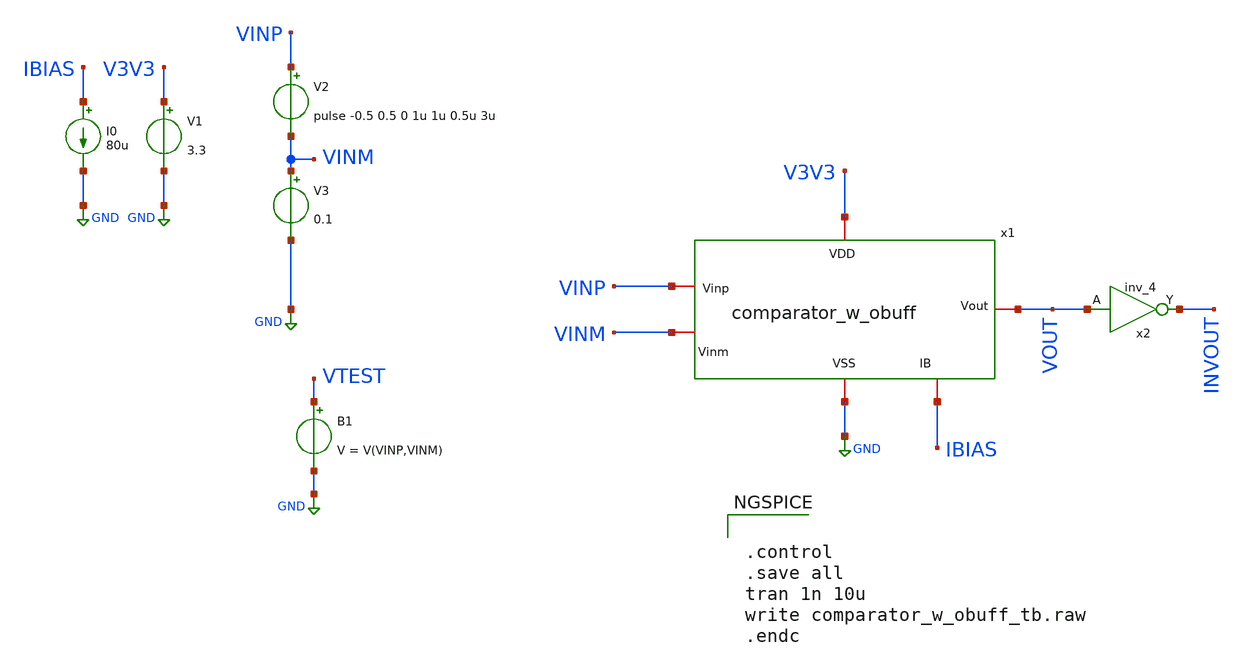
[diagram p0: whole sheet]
** sch_path: design/comparator/comparator_w_obuff_tb.sch
**.subckt comparator_w_obuff_tb
V1 V3V3 GND 3.3
I0 IBIAS GND 80u
V3 VINM GND 0.1
V2 VINP VINM pulse -0.5 0.5 0 1u 1u 0.5u 3u
x2 VOUT GND GND V3V3 V3V3 INVOUT sky130_fd_sc_hvl__inv_4
B1 VTEST GND V = V(VINP,VINM)
x1 V3V3 GND VOUT VINP VINM IBIAS comparator_w_obuff
**** begin user architecture code

.include $::SKYWATER_MODELS/cells/nfet_01v8/sky130_fd_pr__nfet_01v8__tt.corner.spice
.include $::SKYWATER_MODELS/cells/nfet_01v8_lvt/sky130_fd_pr__nfet_01v8_lvt__tt.corner.spice
.include $::SKYWATER_MODELS/cells/pfet_01v8/sky130_fd_pr__pfet_01v8__tt.corner.spice
.include $::SKYWATER_MODELS/cells/nfet_03v3_nvt/sky130_fd_pr__nfet_03v3_nvt__tt.corner.spice
.include $::SKYWATER_MODELS/cells/nfet_05v0_nvt/sky130_fd_pr__nfet_05v0_nvt__tt.corner.spice
.include $::SKYWATER_MODELS/cells/esd_nfet_01v8/sky130_fd_pr__esd_nfet_01v8__tt.corner.spice
.include $::SKYWATER_MODELS/cells/pfet_01v8_lvt/sky130_fd_pr__pfet_01v8_lvt__tt.corner.spice
.include $::SKYWATER_MODELS/cells/pfet_01v8_hvt/sky130_fd_pr__pfet_01v8_hvt__tt.corner.spice
.include $::SKYWATER_MODELS/cells/esd_pfet_g5v0d10v5/sky130_fd_pr__esd_pfet_g5v0d10v5__tt.corner.spice
.include $::SKYWATER_MODELS/cells/pfet_g5v0d10v5/sky130_fd_pr__pfet_g5v0d10v5__tt.corner.spice
.include $::SKYWATER_MODELS/cells/pfet_g5v0d16v0/sky130_fd_pr__pfet_g5v0d16v0__tt.corner.spice
.include $::SKYWATER_MODELS/cells/nfet_g5v0d10v5/sky130_fd_pr__nfet_g5v0d10v5__tt.corner.spice
.include $::SKYWATER_MODELS/cells/nfet_g5v0d16v0/sky130_fd_pr__nfet_g5v0d16v0__tt_discrete.corner.spice
.include $::SKYWATER_MODELS/cells/esd_nfet_g5v0d10v5/sky130_fd_pr__esd_nfet_g5v0d10v5__tt.corner.spice
.include $::SKYWATER_MODELS/models/corners/tt/nonfet.spice
* Mismatch parameters
.include $::SKYWATER_MODELS/cells/nfet_01v8/sky130_fd_pr__nfet_01v8__mismatch.corner.spice
.include $::SKYWATER_MODELS/cells/pfet_01v8/sky130_fd_pr__pfet_01v8__mismatch.corner.spice
.include $::SKYWATER_MODELS/cells/nfet_01v8_lvt/sky130_fd_pr__nfet_01v8_lvt__mismatch.corner.spice
.include $::SKYWATER_MODELS/cells/pfet_01v8_lvt/sky130_fd_pr__pfet_01v8_lvt__mismatch.corner.spice
.include $::SKYWATER_MODELS/cells/pfet_01v8_hvt/sky130_fd_pr__pfet_01v8_hvt__mismatch.corner.spice
.include $::SKYWATER_MODELS/cells/nfet_g5v0d10v5/sky130_fd_pr__nfet_g5v0d10v5__mismatch.corner.spice
.include $::SKYWATER_MODELS/cells/pfet_g5v0d10v5/sky130_fd_pr__pfet_g5v0d10v5__mismatch.corner.spice
.include $::SKYWATER_MODELS/cells/nfet_05v0_nvt/sky130_fd_pr__nfet_05v0_nvt__mismatch.corner.spice
.include $::SKYWATER_MODELS/cells/nfet_03v3_nvt/sky130_fd_pr__nfet_03v3_nvt__mismatch.corner.spice
* Resistor$::SKYWATER_MODELS/Capacitor
.include $::SKYWATER_MODELS/models/r+c/res_typical__cap_typical.spice
.include $::SKYWATER_MODELS/models/r+c/res_typical__cap_typical__lin.spice
* Special cells
.include $::SKYWATER_MODELS/models/corners/tt/specialized_cells.spice
* All models
.include $::SKYWATER_MODELS/models/all.spice
* Corner
.include $::SKYWATER_MODELS/models/corners/tt/rf.spice



.control
.save all
tran 1n 10u
write comparator_w_obuff_tb.raw
.endc


**** end user architecture code
**.ends

* expanding   symbol:  design/comparator/comparator_w_obuff.sym # of pins=6
** sym_path: design/comparator/comparator_w_obuff.sym
** sch_path: design/comparator/comparator_w_obuff.sch
.subckt comparator_w_obuff VDD VSS Vout Vinp Vinm IB
*.iopin VDD
*.iopin VSS
*.iopin Vout
*.iopin Vinp
*.iopin Vinm
*.iopin IB
XM11 net4 IB VDD VDD sky130_fd_pr__pfet_g5v0d10v5 L=1 W=5 nf=1 ad='int((nf+1)/2) * W/nf * 0.29' as='int((nf+2)/2) * W/nf * 0.29'
+ pd='2*int((nf+1)/2) * (W/nf + 0.29)' ps='2*int((nf+2)/2) * (W/nf + 0.29)' nrd='0.29 / W' nrs='0.29 / W'
+ sa=0 sb=0 sd=0 mult=4 m=4
XM8 VMID net1 VDD VDD sky130_fd_pr__pfet_g5v0d10v5 L=1 W=5 nf=1 ad='int((nf+1)/2) * W/nf * 0.29' as='int((nf+2)/2) * W/nf * 0.29'
+ pd='2*int((nf+1)/2) * (W/nf + 0.29)' ps='2*int((nf+2)/2) * (W/nf + 0.29)' nrd='0.29 / W' nrs='0.29 / W'
+ sa=0 sb=0 sd=0 mult=4 m=4
XM7 net1 net1 VDD VDD sky130_fd_pr__pfet_g5v0d10v5 L=1 W=5 nf=1 ad='int((nf+1)/2) * W/nf * 0.29' as='int((nf+2)/2) * W/nf * 0.29'
+ pd='2*int((nf+1)/2) * (W/nf + 0.29)' ps='2*int((nf+2)/2) * (W/nf + 0.29)' nrd='0.29 / W' nrs='0.29 / W'
+ sa=0 sb=0 sd=0 mult=4 m=4
XM2 net3 Vinm net4 VDD sky130_fd_pr__pfet_g5v0d10v5 L=1 W=5 nf=1 ad='int((nf+1)/2) * W/nf * 0.29' as='int((nf+2)/2) * W/nf * 0.29'
+ pd='2*int((nf+1)/2) * (W/nf + 0.29)' ps='2*int((nf+2)/2) * (W/nf + 0.29)' nrd='0.29 / W' nrs='0.29 / W'
+ sa=0 sb=0 sd=0 mult=4 m=4
XM1 net2 Vinp net4 VDD sky130_fd_pr__pfet_g5v0d10v5 L=1 W=5 nf=1 ad='int((nf+1)/2) * W/nf * 0.29' as='int((nf+2)/2) * W/nf * 0.29'
+ pd='2*int((nf+1)/2) * (W/nf + 0.29)' ps='2*int((nf+2)/2) * (W/nf + 0.29)' nrd='0.29 / W' nrs='0.29 / W'
+ sa=0 sb=0 sd=0 mult=4 m=4
XMmir IB IB VDD VDD sky130_fd_pr__pfet_g5v0d10v5 L=1 W=5 nf=1 ad='int((nf+1)/2) * W/nf * 0.29' as='int((nf+2)/2) * W/nf * 0.29'
+ pd='2*int((nf+1)/2) * (W/nf + 0.29)' ps='2*int((nf+2)/2) * (W/nf + 0.29)' nrd='0.29 / W' nrs='0.29 / W'
+ sa=0 sb=0 sd=0 mult=4 m=4
XM12 VMID net3 VSS VSS sky130_fd_pr__nfet_g5v0d10v5 L=1 W=5 nf=1 ad='int((nf+1)/2) * W/nf * 0.29' as='int((nf+2)/2) * W/nf * 0.29'
+ pd='2*int((nf+1)/2) * (W/nf + 0.29)' ps='2*int((nf+2)/2) * (W/nf + 0.29)' nrd='0.29 / W' nrs='0.29 / W'
+ sa=0 sb=0 sd=0 mult=4 m=4
XM4 net3 net3 VSS VSS sky130_fd_pr__nfet_g5v0d10v5 L=1 W=5 nf=1 ad='int((nf+1)/2) * W/nf * 0.29' as='int((nf+2)/2) * W/nf * 0.29'
+ pd='2*int((nf+1)/2) * (W/nf + 0.29)' ps='2*int((nf+2)/2) * (W/nf + 0.29)' nrd='0.29 / W' nrs='0.29 / W'
+ sa=0 sb=0 sd=0 mult=3 m=3
XM6 net2 net3 VSS VSS sky130_fd_pr__nfet_g5v0d10v5 L=1 W=5 nf=1 ad='int((nf+1)/2) * W/nf * 0.29' as='int((nf+2)/2) * W/nf * 0.29'
+ pd='2*int((nf+1)/2) * (W/nf + 0.29)' ps='2*int((nf+2)/2) * (W/nf + 0.29)' nrd='0.29 / W' nrs='0.29 / W'
+ sa=0 sb=0 sd=0 mult=4 m=4
XM5 net3 net2 VSS VSS sky130_fd_pr__nfet_g5v0d10v5 L=1 W=5 nf=1 ad='int((nf+1)/2) * W/nf * 0.29' as='int((nf+2)/2) * W/nf * 0.29'
+ pd='2*int((nf+1)/2) * (W/nf + 0.29)' ps='2*int((nf+2)/2) * (W/nf + 0.29)' nrd='0.29 / W' nrs='0.29 / W'
+ sa=0 sb=0 sd=0 mult=4 m=4
XM3 net2 net2 VSS VSS sky130_fd_pr__nfet_g5v0d10v5 L=1 W=5 nf=1 ad='int((nf+1)/2) * W/nf * 0.29' as='int((nf+2)/2) * W/nf * 0.29'
+ pd='2*int((nf+1)/2) * (W/nf + 0.29)' ps='2*int((nf+2)/2) * (W/nf + 0.29)' nrd='0.29 / W' nrs='0.29 / W'
+ sa=0 sb=0 sd=0 mult=3 m=3
XM9 net1 net2 VSS VSS sky130_fd_pr__nfet_g5v0d10v5 L=1 W=5 nf=1 ad='int((nf+1)/2) * W/nf * 0.29' as='int((nf+2)/2) * W/nf * 0.29'
+ pd='2*int((nf+1)/2) * (W/nf + 0.29)' ps='2*int((nf+2)/2) * (W/nf + 0.29)' nrd='0.29 / W' nrs='0.29 / W'
+ sa=0 sb=0 sd=0 mult=4 m=4
XM10 Vout VMID VDD VDD sky130_fd_pr__pfet_g5v0d10v5 L=0.5 W=5 nf=1 ad='int((nf+1)/2) * W/nf * 0.29' as='int((nf+2)/2) * W/nf * 0.29'
+ pd='2*int((nf+1)/2) * (W/nf + 0.29)' ps='2*int((nf+2)/2) * (W/nf + 0.29)' nrd='0.29 / W' nrs='0.29 / W'
+ sa=0 sb=0 sd=0 mult=1 m=1
XM13 Vout VMID VSS VSS sky130_fd_pr__nfet_g5v0d10v5 L=0.5 W=5 nf=1 ad='int((nf+1)/2) * W/nf * 0.29' as='int((nf+2)/2) * W/nf * 0.29'
+ pd='2*int((nf+1)/2) * (W/nf + 0.29)' ps='2*int((nf+2)/2) * (W/nf + 0.29)' nrd='0.29 / W' nrs='0.29 / W'
+ sa=0 sb=0 sd=0 mult=1 m=1
.ends

.GLOBAL GND
**** begin user architecture code
[sky130_models]
**** end user architecture code
.end
